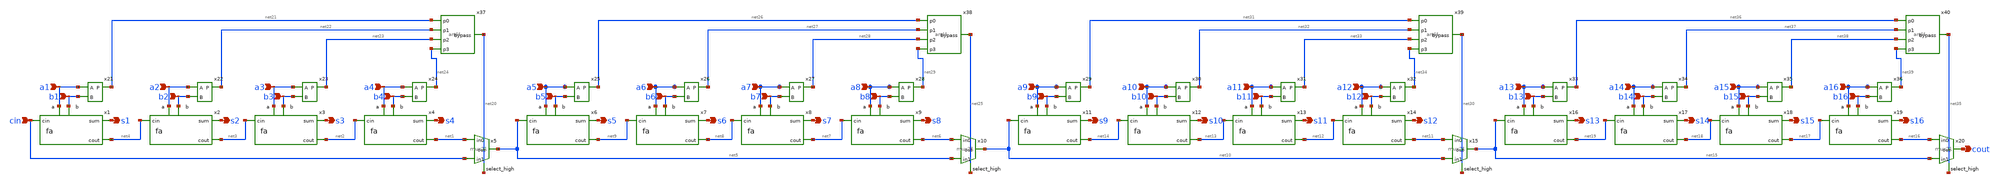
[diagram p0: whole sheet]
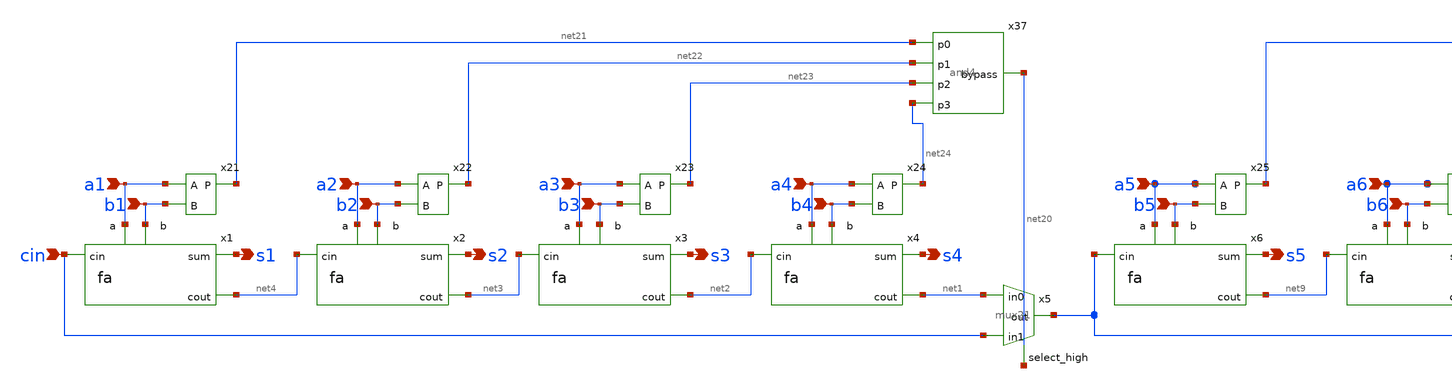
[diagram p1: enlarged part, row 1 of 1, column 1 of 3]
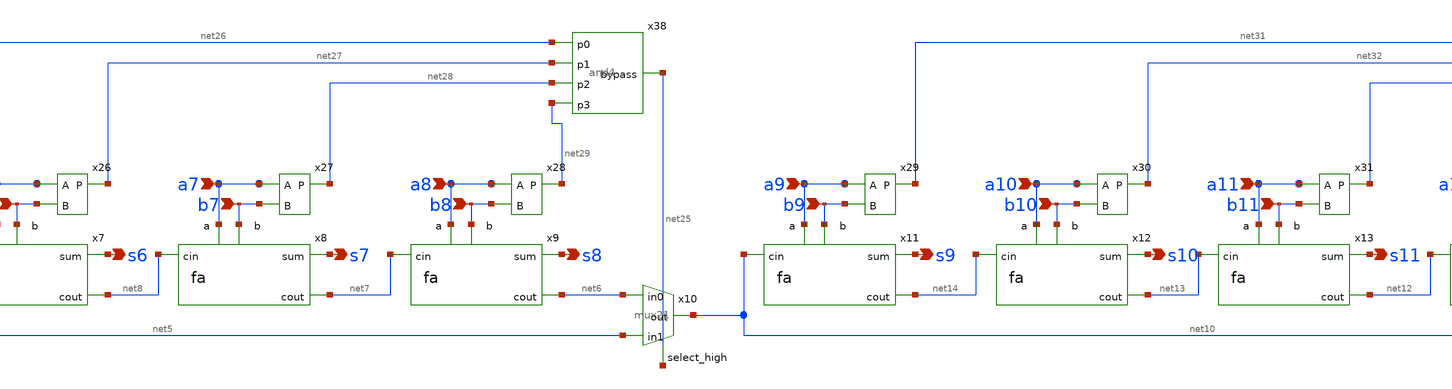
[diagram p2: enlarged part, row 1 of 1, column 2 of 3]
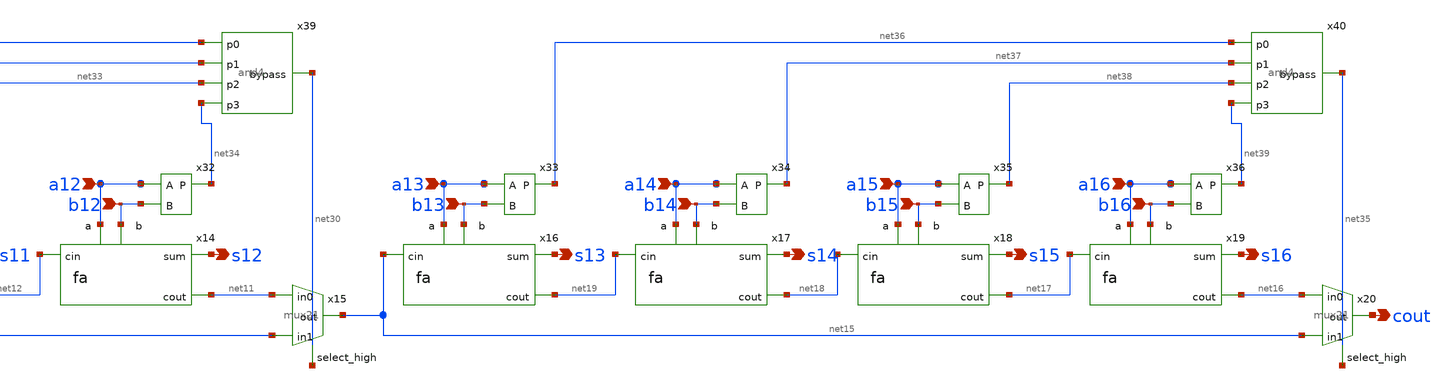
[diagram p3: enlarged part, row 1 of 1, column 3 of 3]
** sch_path: tut9/cba16.sch
**.subckt cba16 s1 s2 s3 s4 s5 s6 s7 s8 s9 s10 s11 s12 s13 s14 s15 s16 cout a1 b1 a2 b2 a3 b3 a4 b4
*+ a5 b5 a6 b6 a7 b7 a8 b8 a9 b9 a10 b10 a11 b11 a12 b12 a13 b13 a14 b14 a15 b15 a16 b16 cin
*.opin s1
*.opin s2
*.opin s3
*.opin s4
*.opin s5
*.opin s6
*.opin s7
*.opin s8
*.opin s9
*.opin s10
*.opin s11
*.opin s12
*.opin s13
*.opin s14
*.opin s15
*.opin s16
*.opin cout
*.ipin a1
*.ipin b1
*.ipin a2
*.ipin b2
*.ipin a3
*.ipin b3
*.ipin a4
*.ipin b4
*.ipin a5
*.ipin b5
*.ipin a6
*.ipin b6
*.ipin a7
*.ipin b7
*.ipin a8
*.ipin b8
*.ipin a9
*.ipin b9
*.ipin a10
*.ipin b10
*.ipin a11
*.ipin b11
*.ipin a12
*.ipin b12
*.ipin a13
*.ipin b13
*.ipin a14
*.ipin b14
*.ipin a15
*.ipin b15
*.ipin a16
*.ipin b16
*.ipin cin
x1 a1 s1 b1 net4 cin fa
x2 a2 s2 b2 net3 net4 fa
x3 a3 s3 b3 net2 net3 fa
x4 a4 s4 b4 net1 net2 fa
x5 net1 cin net5 net20 mux21
x6 a5 s5 b5 net9 net5 fa
x7 a6 s6 b6 net8 net9 fa
x8 a7 s7 b7 net7 net8 fa
x9 a8 s8 b8 net6 net7 fa
x10 net6 net5 net10 net25 mux21
x11 a9 s9 b9 net14 net10 fa
x12 a10 s10 b10 net13 net14 fa
x13 a11 s11 b11 net12 net13 fa
x14 a12 s12 b12 net11 net12 fa
x15 net11 net10 net15 net30 mux21
x16 a13 s13 b13 net19 net15 fa
x17 a14 s14 b14 net18 net19 fa
x18 a15 s15 b15 net17 net18 fa
x19 a16 s16 b16 net16 net17 fa
x20 net16 net15 cout net35 mux21
x21 a1 net21 b1 P
x22 a2 net22 b2 P
x23 a3 net23 b3 P
x24 a4 net24 b4 P
x25 a5 net26 b5 P
x26 a6 net27 b6 P
x27 a7 net28 b7 P
x28 a8 net29 b8 P
x29 a9 net31 b9 P
x30 a10 net32 b10 P
x31 a11 net33 b11 P
x32 a12 net34 b12 P
x33 a13 net36 b13 P
x34 a14 net37 b14 P
x35 a15 net38 b15 P
x36 a16 net39 b16 P
x37 net21 net22 net20 net23 net24 and4
x38 net26 net27 net25 net28 net29 and4
x39 net31 net32 net30 net33 net34 and4
x40 net36 net37 net35 net38 net39 and4
**.ends
.end
